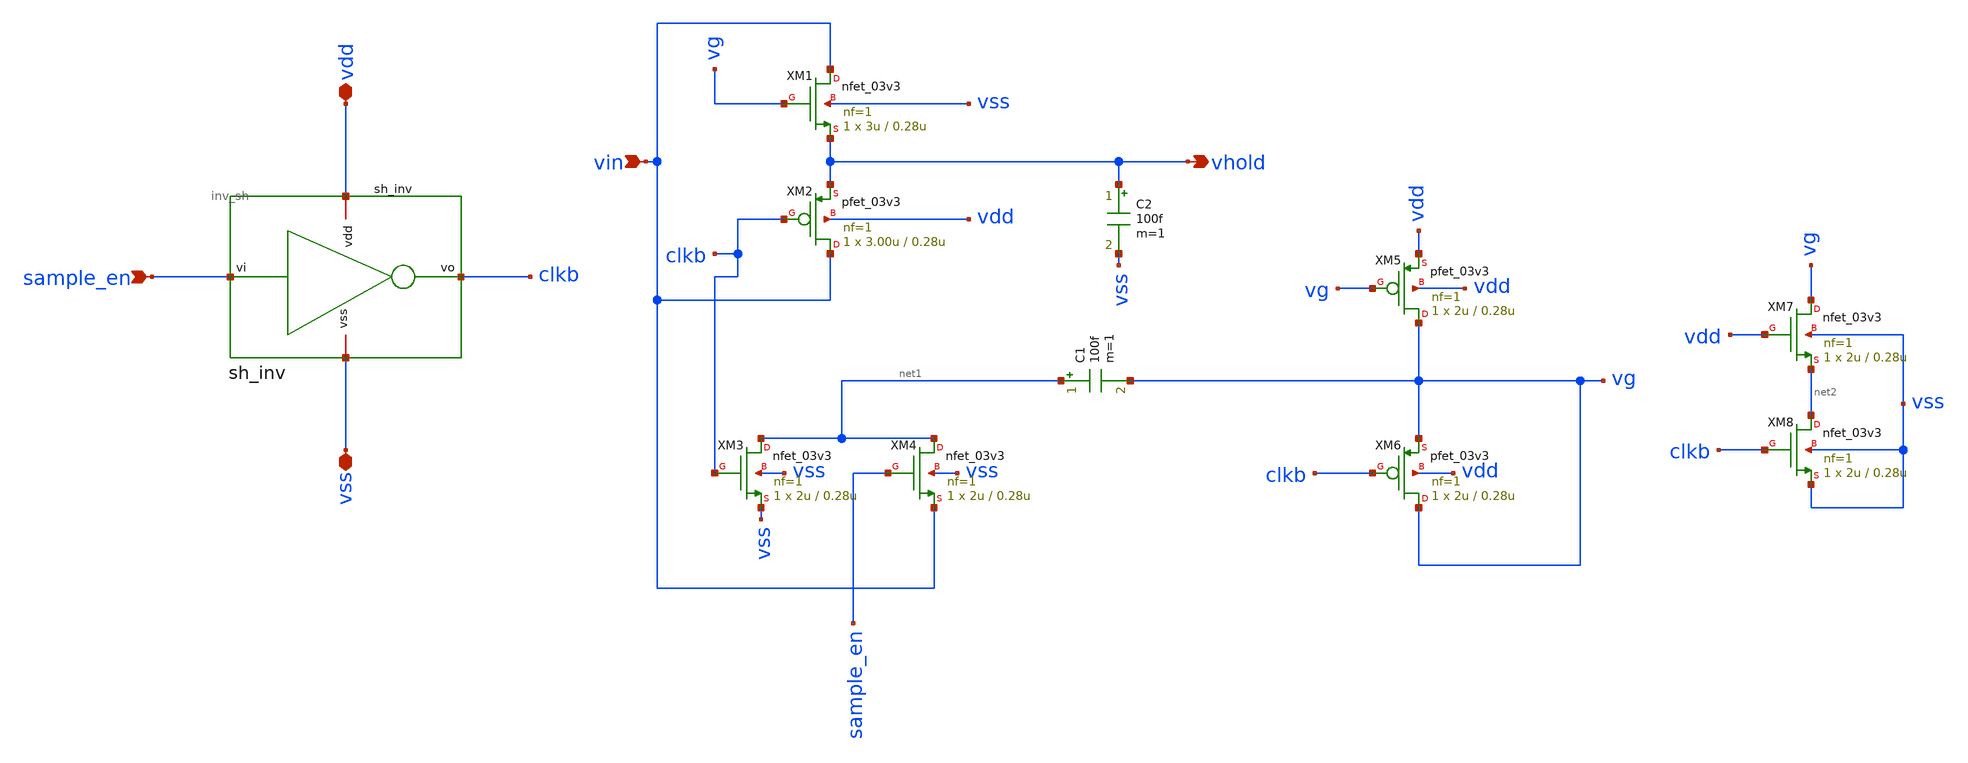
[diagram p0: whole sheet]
** sch_path: xschem/sar_adc/blocks/sample_hold/sample_hold.sch
**.subckt sample_hold vin sample_en vhold vdd vss
*.ipin vin
*.ipin sample_en
*.opin vhold
*.iopin vdd
*.iopin vss
C1 net1 vg 100f m=1
C2 vhold vss 100f m=1
XM1 vin vg vhold vss nfet_03v3 L=0.28u W=3u nf=1 ad='int((nf+1)/2) * W/nf * 0.18u' as='int((nf+2)/2) * W/nf * 0.18u'
+ pd='2*int((nf+1)/2) * (W/nf + 0.18u)' ps='2*int((nf+2)/2) * (W/nf + 0.18u)' nrd='0.18u / W' nrs='0.18u / W'
+ sa=0 sb=0 sd=0 m=1
XM2 vin clkb vhold vdd pfet_03v3 L=0.28u W=3.00u nf=1 ad='int((nf+1)/2) * W/nf * 0.18u' as='int((nf+2)/2) * W/nf * 0.18u'
+ pd='2*int((nf+1)/2) * (W/nf + 0.18u)' ps='2*int((nf+2)/2) * (W/nf + 0.18u)' nrd='0.18u / W' nrs='0.18u / W'
+ sa=0 sb=0 sd=0 m=1
XM3 net1 clkb vss vss nfet_03v3 L=0.28u W=2u nf=1 ad='int((nf+1)/2) * W/nf * 0.18u' as='int((nf+2)/2) * W/nf * 0.18u'
+ pd='2*int((nf+1)/2) * (W/nf + 0.18u)' ps='2*int((nf+2)/2) * (W/nf + 0.18u)' nrd='0.18u / W' nrs='0.18u / W'
+ sa=0 sb=0 sd=0 m=1
XM4 net1 sample_en vin vss nfet_03v3 L=0.28u W=2u nf=1 ad='int((nf+1)/2) * W/nf * 0.18u' as='int((nf+2)/2) * W/nf * 0.18u'
+ pd='2*int((nf+1)/2) * (W/nf + 0.18u)' ps='2*int((nf+2)/2) * (W/nf + 0.18u)' nrd='0.18u / W' nrs='0.18u / W'
+ sa=0 sb=0 sd=0 m=1
XM5 vg vg vdd vdd pfet_03v3 L=0.28u W=2u nf=1 ad='int((nf+1)/2) * W/nf * 0.18u' as='int((nf+2)/2) * W/nf * 0.18u'
+ pd='2*int((nf+1)/2) * (W/nf + 0.18u)' ps='2*int((nf+2)/2) * (W/nf + 0.18u)' nrd='0.18u / W' nrs='0.18u / W'
+ sa=0 sb=0 sd=0 m=1
XM6 vg clkb vg vdd pfet_03v3 L=0.28u W=2u nf=1 ad='int((nf+1)/2) * W/nf * 0.18u' as='int((nf+2)/2) * W/nf * 0.18u'
+ pd='2*int((nf+1)/2) * (W/nf + 0.18u)' ps='2*int((nf+2)/2) * (W/nf + 0.18u)' nrd='0.18u / W' nrs='0.18u / W'
+ sa=0 sb=0 sd=0 m=1
XM7 vg vdd net2 vss nfet_03v3 L=0.28u W=2u nf=1 ad='int((nf+1)/2) * W/nf * 0.18u' as='int((nf+2)/2) * W/nf * 0.18u'
+ pd='2*int((nf+1)/2) * (W/nf + 0.18u)' ps='2*int((nf+2)/2) * (W/nf + 0.18u)' nrd='0.18u / W' nrs='0.18u / W'
+ sa=0 sb=0 sd=0 m=1
XM8 net2 clkb vss vss nfet_03v3 L=0.28u W=2u nf=1 ad='int((nf+1)/2) * W/nf * 0.18u' as='int((nf+2)/2) * W/nf * 0.18u'
+ pd='2*int((nf+1)/2) * (W/nf + 0.18u)' ps='2*int((nf+2)/2) * (W/nf + 0.18u)' nrd='0.18u / W' nrs='0.18u / W'
+ sa=0 sb=0 sd=0 m=1
xinv2 vdd clkb sample_en vss inv_sh
**.ends

* expanding   symbol:  sar_adc/blocks/sample_hold/inv_sh.sym # of pins=4
** sym_path: xschem/sar_adc/blocks/sample_hold/inv_sh.sym
** sch_path: xschem/sar_adc/blocks/sample_hold/inv_sh.sch
.subckt inv_sh vdd vo vi vss
*.iopin vdd
*.ipin vi
*.opin vo
*.iopin vss
XM1 vo vi vss vss nfet_03v3 L=0.28u W=1u nf=1 ad='int((nf+1)/2) * W/nf * 0.18u' as='int((nf+2)/2) * W/nf * 0.18u'
+ pd='2*int((nf+1)/2) * (W/nf + 0.18u)' ps='2*int((nf+2)/2) * (W/nf + 0.18u)' nrd='0.18u / W' nrs='0.18u / W'
+ sa=0 sb=0 sd=0 m=1
XM2 vo vi vdd vdd pfet_03v3 L=0.28u W=2u nf=1 ad='int((nf+1)/2) * W/nf * 0.18u' as='int((nf+2)/2) * W/nf * 0.18u'
+ pd='2*int((nf+1)/2) * (W/nf + 0.18u)' ps='2*int((nf+2)/2) * (W/nf + 0.18u)' nrd='0.18u / W' nrs='0.18u / W'
+ sa=0 sb=0 sd=0 m=1
.ends

.end
